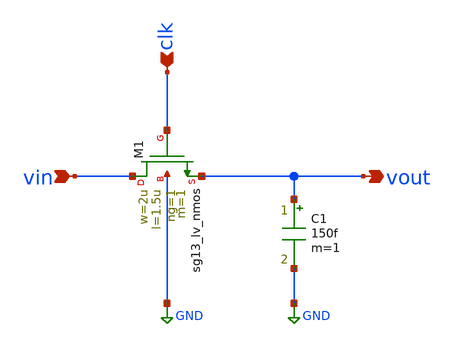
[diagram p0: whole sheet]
** sch_path: schematics/nmos_switch.sch
**.subckt nmos_switch vin clk vout
*.ipin vin
*.ipin clk
*.opin vout
XM1 vin clk vout GND sg13_lv_nmos w=2u l=1.5u ng=1 m=1 mm_ok=1
C1 vout GND 150f m=1
**.ends
.GLOBAL GND
.end
